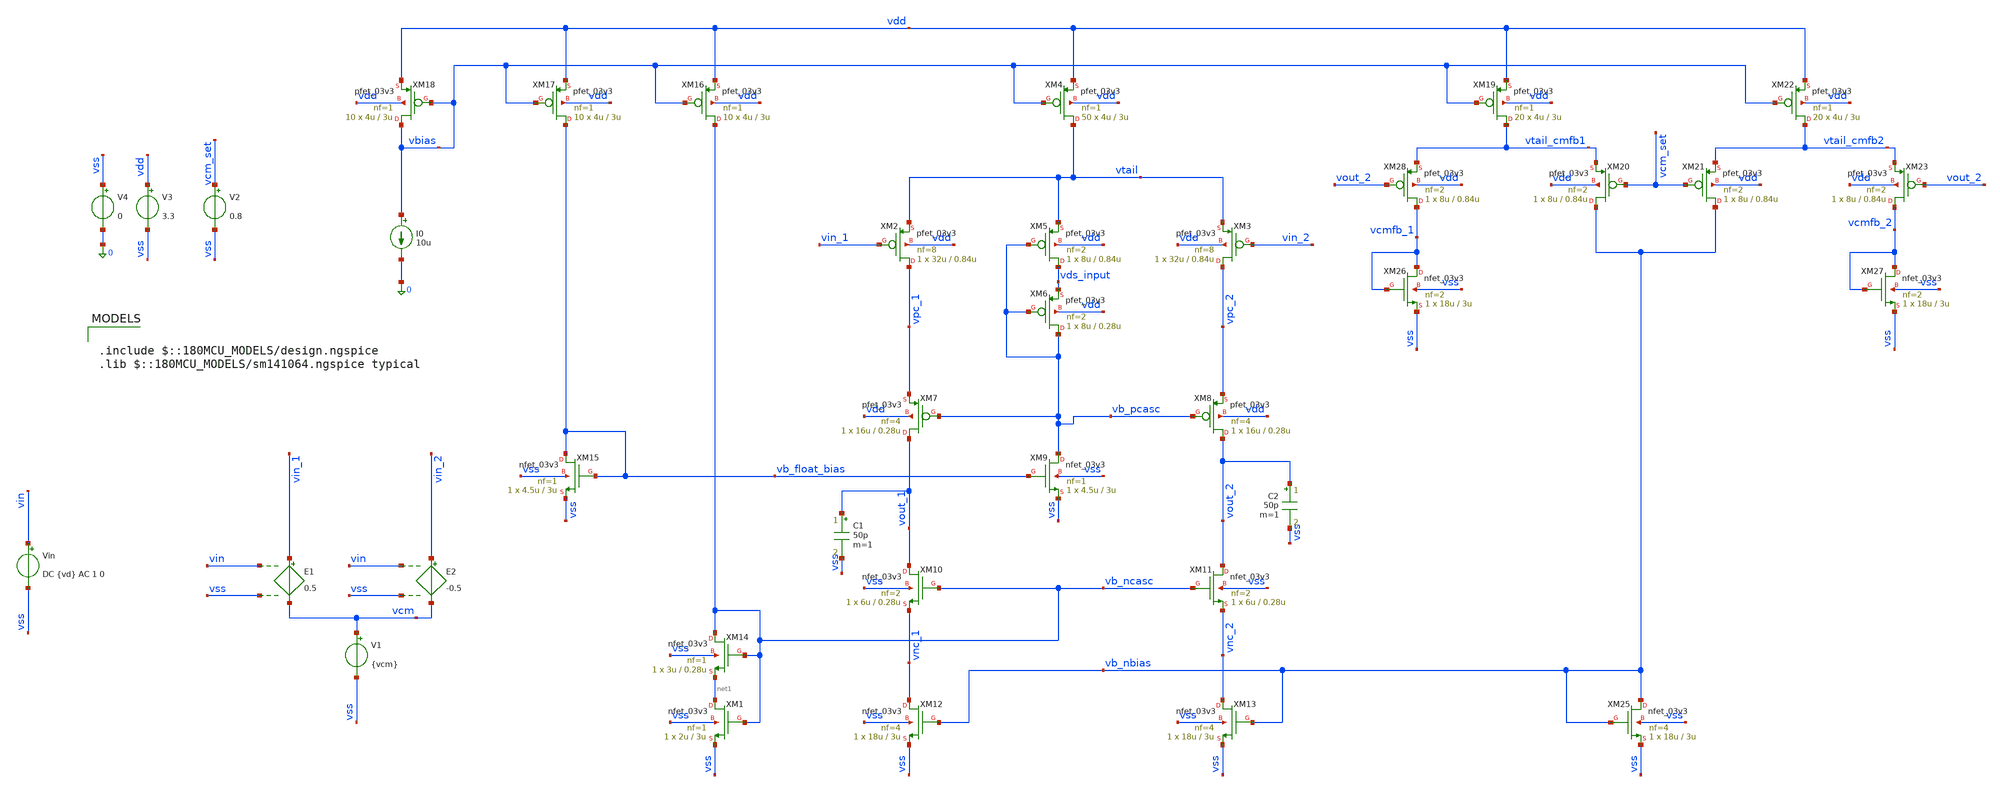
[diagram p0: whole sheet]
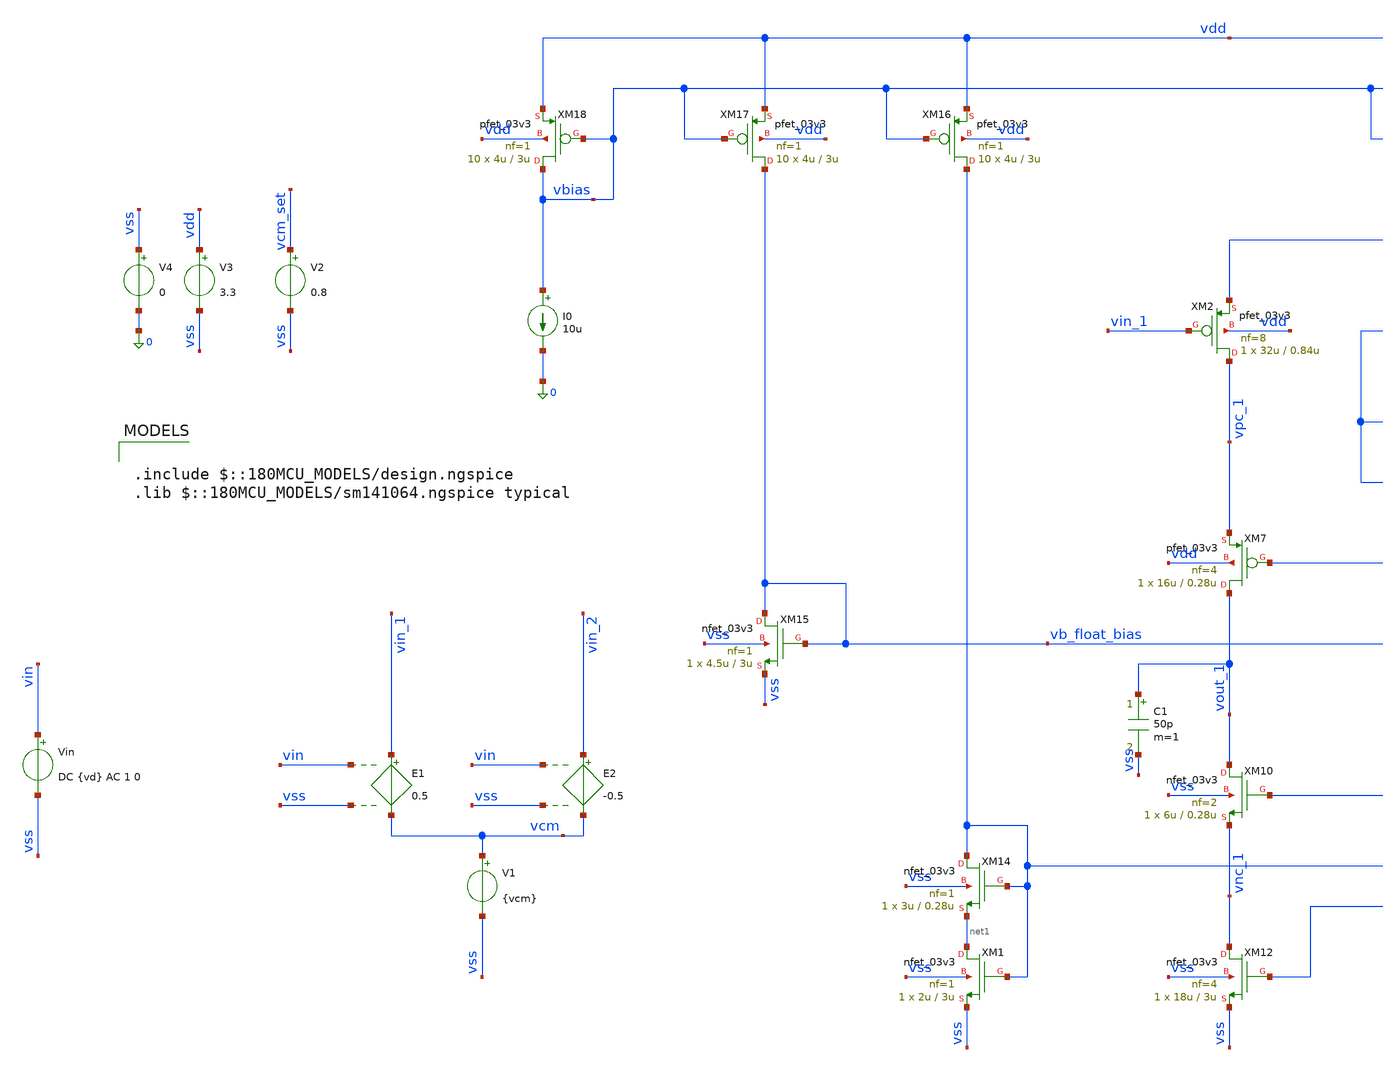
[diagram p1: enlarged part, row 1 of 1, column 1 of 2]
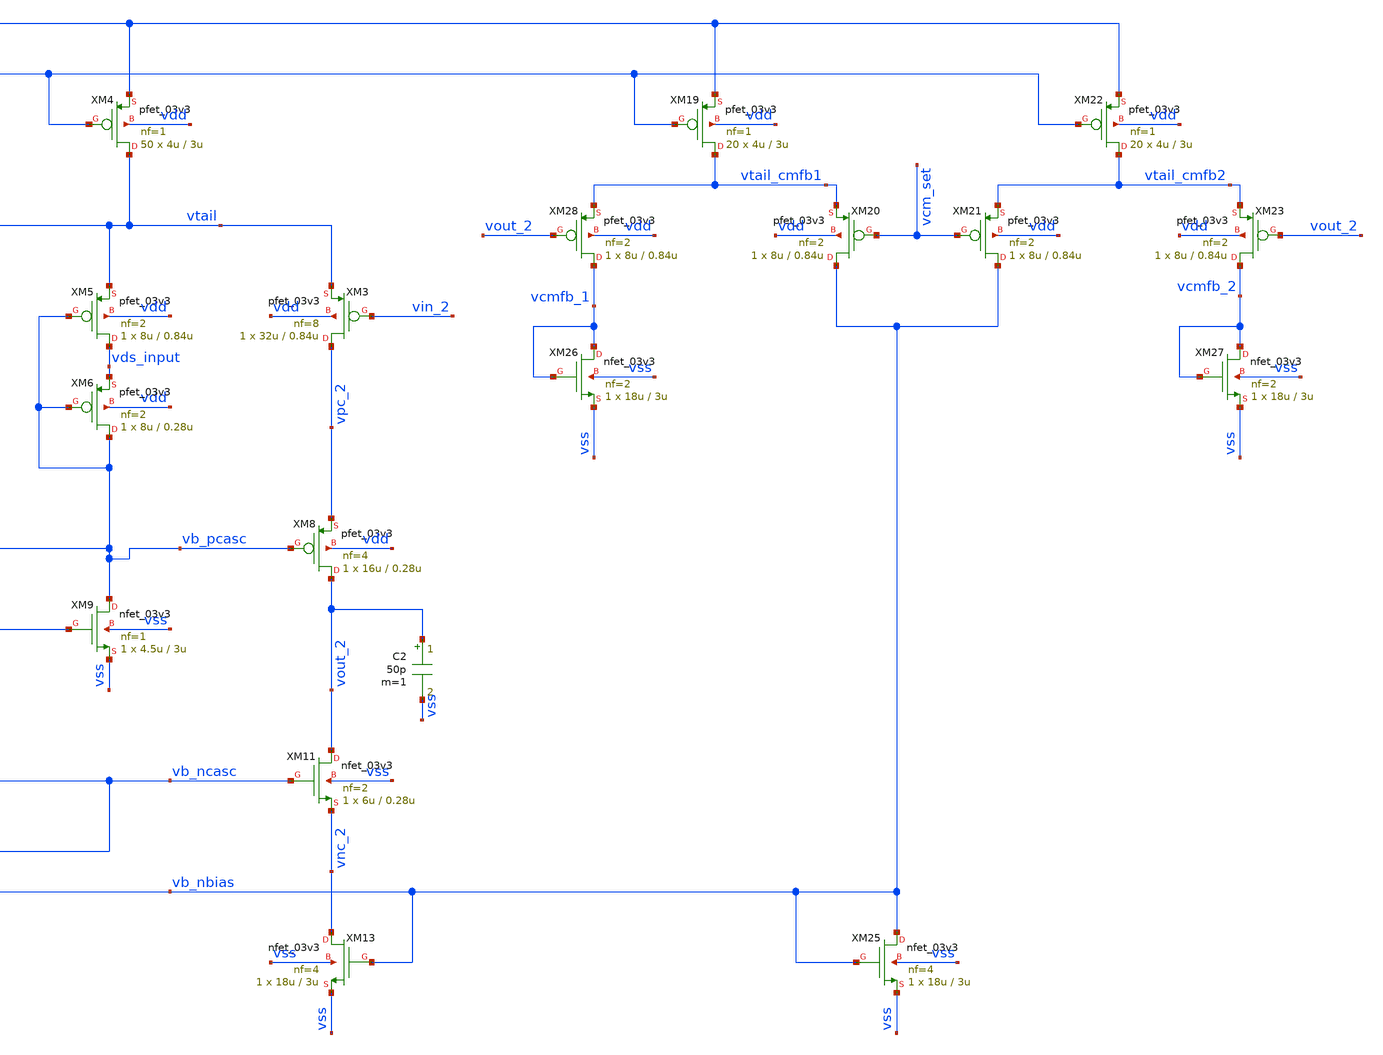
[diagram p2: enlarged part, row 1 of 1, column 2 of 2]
** sch_path: xschem/rrl/telescopic_test.sch
**.subckt telescopic_test
XM2 vpc_1 vin_1 vtail vdd pfet_03v3 L=0.84u W=32u nf=8 ad='int((nf+1)/2) * W/nf * 0.18u' as='int((nf+2)/2) * W/nf * 0.18u'
+ pd='2*int((nf+1)/2) * (W/nf + 0.18u)' ps='2*int((nf+2)/2) * (W/nf + 0.18u)' nrd='0.18u / W' nrs='0.18u / W'
+ sa=0 sb=0 sd=0 m=1
XM4 vtail vbias vdd vdd pfet_03v3 L=3u W=4u nf=1 ad='int((nf+1)/2) * W/nf * 0.18u' as='int((nf+2)/2) * W/nf * 0.18u'
+ pd='2*int((nf+1)/2) * (W/nf + 0.18u)' ps='2*int((nf+2)/2) * (W/nf + 0.18u)' nrd='0.18u / W' nrs='0.18u / W'
+ sa=0 sb=0 sd=0 m=50
XM10 vout_1 vb_ncasc vnc_1 vss nfet_03v3 L=0.28u W=6u nf=2 ad='int((nf+1)/2) * W/nf * 0.18u' as='int((nf+2)/2) * W/nf * 0.18u'
+ pd='2*int((nf+1)/2) * (W/nf + 0.18u)' ps='2*int((nf+2)/2) * (W/nf + 0.18u)' nrd='0.18u / W' nrs='0.18u / W'
+ sa=0 sb=0 sd=0 m=1
XM12 vnc_1 vb_nbias vss vss nfet_03v3 L=3u W=18u nf=4 ad='int((nf+1)/2) * W/nf * 0.18u' as='int((nf+2)/2) * W/nf * 0.18u'
+ pd='2*int((nf+1)/2) * (W/nf + 0.18u)' ps='2*int((nf+2)/2) * (W/nf + 0.18u)' nrd='0.18u / W' nrs='0.18u / W'
+ sa=0 sb=0 sd=0 m=1
XM1 net1 vb_ncasc vss vss nfet_03v3 L=3u W=2u nf=1 ad='int((nf+1)/2) * W/nf * 0.18u' as='int((nf+2)/2) * W/nf * 0.18u'
+ pd='2*int((nf+1)/2) * (W/nf + 0.18u)' ps='2*int((nf+2)/2) * (W/nf + 0.18u)' nrd='0.18u / W' nrs='0.18u / W'
+ sa=0 sb=0 sd=0 m=1
XM5 vds_input vb_pcasc vtail vdd pfet_03v3 L=0.84u W=8u nf=2 ad='int((nf+1)/2) * W/nf * 0.18u' as='int((nf+2)/2) * W/nf * 0.18u'
+ pd='2*int((nf+1)/2) * (W/nf + 0.18u)' ps='2*int((nf+2)/2) * (W/nf + 0.18u)' nrd='0.18u / W' nrs='0.18u / W'
+ sa=0 sb=0 sd=0 m=1
I0 vbias 0 10u
XM3 vpc_2 vin_2 vtail vdd pfet_03v3 L=0.84u W=32u nf=8 ad='int((nf+1)/2) * W/nf * 0.18u' as='int((nf+2)/2) * W/nf * 0.18u'
+ pd='2*int((nf+1)/2) * (W/nf + 0.18u)' ps='2*int((nf+2)/2) * (W/nf + 0.18u)' nrd='0.18u / W' nrs='0.18u / W'
+ sa=0 sb=0 sd=0 m=1
XM11 vout_2 vb_ncasc vnc_2 vss nfet_03v3 L=0.28u W=6u nf=2 ad='int((nf+1)/2) * W/nf * 0.18u' as='int((nf+2)/2) * W/nf * 0.18u'
+ pd='2*int((nf+1)/2) * (W/nf + 0.18u)' ps='2*int((nf+2)/2) * (W/nf + 0.18u)' nrd='0.18u / W' nrs='0.18u / W'
+ sa=0 sb=0 sd=0 m=1
XM16 vb_ncasc vbias vdd vdd pfet_03v3 L=3u W=4u nf=1 ad='int((nf+1)/2) * W/nf * 0.18u' as='int((nf+2)/2) * W/nf * 0.18u'
+ pd='2*int((nf+1)/2) * (W/nf + 0.18u)' ps='2*int((nf+2)/2) * (W/nf + 0.18u)' nrd='0.18u / W' nrs='0.18u / W'
+ sa=0 sb=0 sd=0 m=10
XM17 vb_float_bias vbias vdd vdd pfet_03v3 L=3u W=4u nf=1 ad='int((nf+1)/2) * W/nf * 0.18u' as='int((nf+2)/2) * W/nf * 0.18u'
+ pd='2*int((nf+1)/2) * (W/nf + 0.18u)' ps='2*int((nf+2)/2) * (W/nf + 0.18u)' nrd='0.18u / W' nrs='0.18u / W'
+ sa=0 sb=0 sd=0 m=10
XM18 vbias vbias vdd vdd pfet_03v3 L=3u W=4u nf=1 ad='int((nf+1)/2) * W/nf * 0.18u' as='int((nf+2)/2) * W/nf * 0.18u'
+ pd='2*int((nf+1)/2) * (W/nf + 0.18u)' ps='2*int((nf+2)/2) * (W/nf + 0.18u)' nrd='0.18u / W' nrs='0.18u / W'
+ sa=0 sb=0 sd=0 m=10
XM13 vnc_2 vb_nbias vss vss nfet_03v3 L=3u W=18u nf=4 ad='int((nf+1)/2) * W/nf * 0.18u' as='int((nf+2)/2) * W/nf * 0.18u'
+ pd='2*int((nf+1)/2) * (W/nf + 0.18u)' ps='2*int((nf+2)/2) * (W/nf + 0.18u)' nrd='0.18u / W' nrs='0.18u / W'
+ sa=0 sb=0 sd=0 m=1
XM15 vb_float_bias vb_float_bias vss vss nfet_03v3 L=3u W=4.5u nf=1 ad='int((nf+1)/2) * W/nf * 0.18u'
+ as='int((nf+2)/2) * W/nf * 0.18u' pd='2*int((nf+1)/2) * (W/nf + 0.18u)' ps='2*int((nf+2)/2) * (W/nf + 0.18u)'
+ nrd='0.18u / W' nrs='0.18u / W' sa=0 sb=0 sd=0 m=1
XM9 vb_pcasc vb_float_bias vss vss nfet_03v3 L=3u W=4.5u nf=1 ad='int((nf+1)/2) * W/nf * 0.18u' as='int((nf+2)/2) * W/nf * 0.18u'
+ pd='2*int((nf+1)/2) * (W/nf + 0.18u)' ps='2*int((nf+2)/2) * (W/nf + 0.18u)' nrd='0.18u / W' nrs='0.18u / W'
+ sa=0 sb=0 sd=0 m=1
XM19 vtail_cmfb1 vbias vdd vdd pfet_03v3 L=3u W=4u nf=1 ad='int((nf+1)/2) * W/nf * 0.18u' as='int((nf+2)/2) * W/nf * 0.18u'
+ pd='2*int((nf+1)/2) * (W/nf + 0.18u)' ps='2*int((nf+2)/2) * (W/nf + 0.18u)' nrd='0.18u / W' nrs='0.18u / W'
+ sa=0 sb=0 sd=0 m=20
XM22 vtail_cmfb2 vbias vdd vdd pfet_03v3 L=3u W=4u nf=1 ad='int((nf+1)/2) * W/nf * 0.18u' as='int((nf+2)/2) * W/nf * 0.18u'
+ pd='2*int((nf+1)/2) * (W/nf + 0.18u)' ps='2*int((nf+2)/2) * (W/nf + 0.18u)' nrd='0.18u / W' nrs='0.18u / W'
+ sa=0 sb=0 sd=0 m=20
XM25 vb_nbias vb_nbias vss vss nfet_03v3 L=3u W=18u nf=4 ad='int((nf+1)/2) * W/nf * 0.18u' as='int((nf+2)/2) * W/nf * 0.18u'
+ pd='2*int((nf+1)/2) * (W/nf + 0.18u)' ps='2*int((nf+2)/2) * (W/nf + 0.18u)' nrd='0.18u / W' nrs='0.18u / W'
+ sa=0 sb=0 sd=0 m=1
XM26 vcmfb_1 vcmfb_1 vss vss nfet_03v3 L=3u W=18u nf=2 ad='int((nf+1)/2) * W/nf * 0.18u' as='int((nf+2)/2) * W/nf * 0.18u'
+ pd='2*int((nf+1)/2) * (W/nf + 0.18u)' ps='2*int((nf+2)/2) * (W/nf + 0.18u)' nrd='0.18u / W' nrs='0.18u / W'
+ sa=0 sb=0 sd=0 m=1
XM27 vcmfb_2 vcmfb_2 vss vss nfet_03v3 L=3u W=18u nf=2 ad='int((nf+1)/2) * W/nf * 0.18u' as='int((nf+2)/2) * W/nf * 0.18u'
+ pd='2*int((nf+1)/2) * (W/nf + 0.18u)' ps='2*int((nf+2)/2) * (W/nf + 0.18u)' nrd='0.18u / W' nrs='0.18u / W'
+ sa=0 sb=0 sd=0 m=1
XM28 vcmfb_1 vout_2 vtail_cmfb1 vdd pfet_03v3 L=0.84u W=8u nf=2 ad='int((nf+1)/2) * W/nf * 0.18u' as='int((nf+2)/2) * W/nf * 0.18u'
+ pd='2*int((nf+1)/2) * (W/nf + 0.18u)' ps='2*int((nf+2)/2) * (W/nf + 0.18u)' nrd='0.18u / W' nrs='0.18u / W'
+ sa=0 sb=0 sd=0 m=1
XM20 vb_nbias vcm_set vtail_cmfb1 vdd pfet_03v3 L=0.84u W=8u nf=2 ad='int((nf+1)/2) * W/nf * 0.18u' as='int((nf+2)/2) * W/nf * 0.18u'
+ pd='2*int((nf+1)/2) * (W/nf + 0.18u)' ps='2*int((nf+2)/2) * (W/nf + 0.18u)' nrd='0.18u / W' nrs='0.18u / W'
+ sa=0 sb=0 sd=0 m=1
XM21 vb_nbias vcm_set vtail_cmfb2 vdd pfet_03v3 L=0.84u W=8u nf=2 ad='int((nf+1)/2) * W/nf * 0.18u' as='int((nf+2)/2) * W/nf * 0.18u'
+ pd='2*int((nf+1)/2) * (W/nf + 0.18u)' ps='2*int((nf+2)/2) * (W/nf + 0.18u)' nrd='0.18u / W' nrs='0.18u / W'
+ sa=0 sb=0 sd=0 m=1
XM23 vcmfb_2 vout_2 vtail_cmfb2 vdd pfet_03v3 L=0.84u W=8u nf=2 ad='int((nf+1)/2) * W/nf * 0.18u' as='int((nf+2)/2) * W/nf * 0.18u'
+ pd='2*int((nf+1)/2) * (W/nf + 0.18u)' ps='2*int((nf+2)/2) * (W/nf + 0.18u)' nrd='0.18u / W' nrs='0.18u / W'
+ sa=0 sb=0 sd=0 m=1
XM6 vb_pcasc vb_pcasc vds_input vdd pfet_03v3 L=0.28u W=8u nf=2 ad='int((nf+1)/2) * W/nf * 0.18u' as='int((nf+2)/2) * W/nf * 0.18u'
+ pd='2*int((nf+1)/2) * (W/nf + 0.18u)' ps='2*int((nf+2)/2) * (W/nf + 0.18u)' nrd='0.18u / W' nrs='0.18u / W'
+ sa=0 sb=0 sd=0 m=1
XM7 vout_1 vb_pcasc vpc_1 vdd pfet_03v3 L=0.28u W=16u nf=4 ad='int((nf+1)/2) * W/nf * 0.18u' as='int((nf+2)/2) * W/nf * 0.18u'
+ pd='2*int((nf+1)/2) * (W/nf + 0.18u)' ps='2*int((nf+2)/2) * (W/nf + 0.18u)' nrd='0.18u / W' nrs='0.18u / W'
+ sa=0 sb=0 sd=0 m=1
XM8 vout_2 vb_pcasc vpc_2 vdd pfet_03v3 L=0.28u W=16u nf=4 ad='int((nf+1)/2) * W/nf * 0.18u' as='int((nf+2)/2) * W/nf * 0.18u'
+ pd='2*int((nf+1)/2) * (W/nf + 0.18u)' ps='2*int((nf+2)/2) * (W/nf + 0.18u)' nrd='0.18u / W' nrs='0.18u / W'
+ sa=0 sb=0 sd=0 m=1
XM14 vb_ncasc vb_ncasc net1 vss nfet_03v3 L=0.28u W=3u nf=1 ad='int((nf+1)/2) * W/nf * 0.18u' as='int((nf+2)/2) * W/nf * 0.18u'
+ pd='2*int((nf+1)/2) * (W/nf + 0.18u)' ps='2*int((nf+2)/2) * (W/nf + 0.18u)' nrd='0.18u / W' nrs='0.18u / W'
+ sa=0 sb=0 sd=0 m=1
V3 vdd vss 3.3
V4 vss 0 0
V1 vcm vss {vcm}
E1 vin_1 vcm vin vss 0.5
E2 vin_2 vcm vin vss -0.5
Vin vin vss DC {vd} AC 1 0
V2 vcm_set vss 0.8
C1 vout_1 vss 50p m=1
C2 vout_2 vss 50p m=1
**** begin user architecture code

.include $::180MCU_MODELS/design.ngspice
.lib $::180MCU_MODELS/sm141064.ngspice typical


.param vcm=0.5
.param vd=0
.control
save all
save @m.xm2.m0[id] @m.xm2.m0[gm] @m.xm2.m0[gds] @m.xm2.m0[cdb] @m.xm2.m0[cgs] @m.xm2.m0[csb]
+ @m.xm2.m0[cgd]
save @m.xm4.m0[id] @m.xm4.m0[gm] @m.xm4.m0[gds] @m.xm4.m0[cdb] @m.xm4.m0[cgs] @m.xm4.m0[csb]
+ @m.xm4.m0[cgd]
save @m.xm10.m0[id] @m.xm10.m0[gm] @m.xm10.m0[gds] @m.xm10.m0[cdb] @m.xm10.m0[cgs] @m.xm10.m0[csb]
+ @m.xm10.m0[cgd]
save @m.xm12.m0[id] @m.xm12.m0[gm] @m.xm12.m0[gds] @m.xm12.m0[cdb] @m.xm12.m0[cgs] @m.xm12.m0[csb]
+ @m.xm12.m0[cgd]
save @m.xm1.m0[id] @m.xm1.m0[gm] @m.xm1.m0[gds] @m.xm1.m0[cdb] @m.xm1.m0[cgs] @m.xm1.m0[csb]
+ @m.xm1.m0[cgd]
save @m.xm5.m0[id] @m.xm5.m0[gm] @m.xm5.m0[gds] @m.xm5.m0[cdb] @m.xm5.m0[cgs] @m.xm5.m0[csb]
+ @m.xm5.m0[cgd]
save @m.xm3.m0[id] @m.xm3.m0[gm] @m.xm3.m0[gds] @m.xm3.m0[cdb] @m.xm3.m0[cgs] @m.xm3.m0[csb]
+ @m.xm3.m0[cgd]
save @m.xm11.m0[id] @m.xm11.m0[gm] @m.xm11.m0[gds] @m.xm11.m0[cdb] @m.xm11.m0[cgs] @m.xm11.m0[csb]
+ @m.xm11.m0[cgd]
save @m.xm16.m0[id] @m.xm16.m0[gm] @m.xm16.m0[gds] @m.xm16.m0[cdb] @m.xm16.m0[cgs] @m.xm16.m0[csb]
+ @m.xm16.m0[cgd]
save @m.xm17.m0[id] @m.xm17.m0[gm] @m.xm17.m0[gds] @m.xm17.m0[cdb] @m.xm17.m0[cgs] @m.xm17.m0[csb]
+ @m.xm17.m0[cgd]
save @m.xm18.m0[id] @m.xm18.m0[gm] @m.xm18.m0[gds] @m.xm18.m0[cdb] @m.xm18.m0[cgs] @m.xm18.m0[csb]
+ @m.xm18.m0[cgd]
save @m.xm13.m0[id] @m.xm13.m0[gm] @m.xm13.m0[gds] @m.xm13.m0[cdb] @m.xm13.m0[cgs] @m.xm13.m0[csb]
+ @m.xm13.m0[cgd]
save @m.xm15.m0[id] @m.xm15.m0[gm] @m.xm15.m0[gds] @m.xm15.m0[cdb] @m.xm15.m0[cgs] @m.xm15.m0[csb]
+ @m.xm15.m0[cgd]
save @m.xm9.m0[id] @m.xm9.m0[gm] @m.xm9.m0[gds] @m.xm9.m0[cdb] @m.xm9.m0[cgs] @m.xm9.m0[csb]
+ @m.xm9.m0[cgd]
save @m.xm19.m0[id] @m.xm19.m0[gm] @m.xm19.m0[gds] @m.xm19.m0[cdb] @m.xm19.m0[cgs] @m.xm19.m0[csb]
+ @m.xm19.m0[cgd]
save @m.xm22.m0[id] @m.xm22.m0[gm] @m.xm22.m0[gds] @m.xm22.m0[cdb] @m.xm22.m0[cgs] @m.xm22.m0[csb]
+ @m.xm22.m0[cgd]
save @m.xm25.m0[id] @m.xm25.m0[gm] @m.xm25.m0[gds] @m.xm25.m0[cdb] @m.xm25.m0[cgs] @m.xm25.m0[csb]
+ @m.xm25.m0[cgd]
save @m.xm26.m0[id] @m.xm26.m0[gm] @m.xm26.m0[gds] @m.xm26.m0[cdb] @m.xm26.m0[cgs] @m.xm26.m0[csb]
+ @m.xm26.m0[cgd]
save @m.xm27.m0[id] @m.xm27.m0[gm] @m.xm27.m0[gds] @m.xm27.m0[cdb] @m.xm27.m0[cgs] @m.xm27.m0[csb]
+ @m.xm27.m0[cgd]
save @m.xm28.m0[id] @m.xm28.m0[gm] @m.xm28.m0[gds] @m.xm28.m0[cdb] @m.xm28.m0[cgs] @m.xm28.m0[csb]
+ @m.xm28.m0[cgd]
save @m.xm20.m0[id] @m.xm20.m0[gm] @m.xm20.m0[gds] @m.xm20.m0[cdb] @m.xm20.m0[cgs] @m.xm20.m0[csb]
+ @m.xm20.m0[cgd]
save @m.xm21.m0[id] @m.xm21.m0[gm] @m.xm21.m0[gds] @m.xm21.m0[cdb] @m.xm21.m0[cgs] @m.xm21.m0[csb]
+ @m.xm21.m0[cgd]
save @m.xm23.m0[id] @m.xm23.m0[gm] @m.xm23.m0[gds] @m.xm23.m0[cdb] @m.xm23.m0[cgs] @m.xm23.m0[csb]
+ @m.xm23.m0[cgd]
save @m.xm6.m0[id] @m.xm6.m0[gm] @m.xm6.m0[gds] @m.xm6.m0[cdb] @m.xm6.m0[cgs] @m.xm6.m0[csb]
+ @m.xm6.m0[cgd]
save @m.xm7.m0[id] @m.xm7.m0[gm] @m.xm7.m0[gds] @m.xm7.m0[cdb] @m.xm7.m0[cgs] @m.xm7.m0[csb]
+ @m.xm7.m0[cgd]
save @m.xm8.m0[id] @m.xm8.m0[gm] @m.xm8.m0[gds] @m.xm8.m0[cdb] @m.xm8.m0[cgs] @m.xm8.m0[csb]
+ @m.xm8.m0[cgd]
save @m.xm14.m0[id] @m.xm14.m0[gm] @m.xm14.m0[gds] @m.xm14.m0[cdb] @m.xm14.m0[cgs] @m.xm14.m0[csb]
+ @m.xm14.m0[cgd]
op
write results_op.raw all
ac dec 100 1 10G
.endc

**** end user architecture code
**.ends
.end
